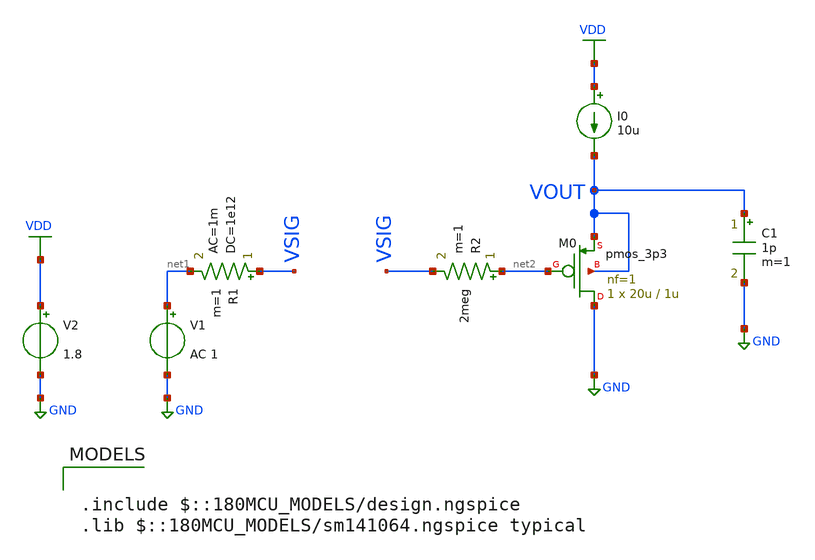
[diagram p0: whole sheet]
** sch_path: ITI_Labs/Lab4/Design/Lab04.sch
**.subckt Lab04
V1 net1 GND AC 1
R1 VSIG net1 1e12 ac=1m m=1
I0 VDD VOUT 10u
V2 VDD GND 1.8
R2 net2 VSIG 2meg m=1
XM0 GND net2 VOUT VOUT pmos_3p3 L=1u W=20u nf=1 ad='int((nf+1)/2) * W/nf * 0.18u' as='int((nf+2)/2) * W/nf * 0.18u'
+ pd='2*int((nf+1)/2) * (W/nf + 0.18u)' ps='2*int((nf+2)/2) * (W/nf + 0.18u)' nrd='0.18u / W' nrs='0.18u / W'
+ sa=0 sb=0 sd=0 m=1
C1 VOUT GND 1p m=1
**** begin user architecture code

.include $::180MCU_MODELS/design.ngspice
.lib $::180MCU_MODELS/sm141064.ngspice typical



.include sim_script.sim


**** end user architecture code
**.ends
.GLOBAL GND
.GLOBAL VDD
.end
